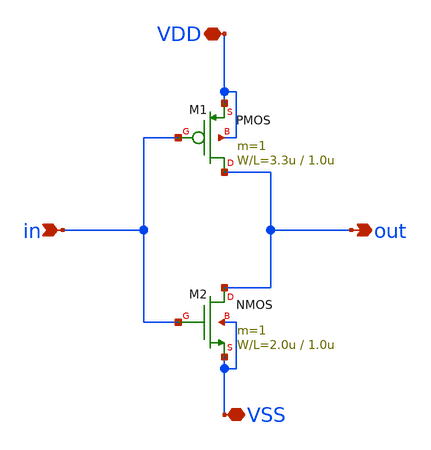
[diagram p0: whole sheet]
** sch_path: samples/inverter/PTS06/inverter.sch
**.subckt inverter in out VDD VSS
*.ipin in
*.opin out
*.iopin VDD
*.iopin VSS
M2 out in VSS VSS NMOS L=1.0u W=2.0u m=1
M1 out in VDD VDD PMOS L=1.0u W=3.3u m=1
**.ends
.end
